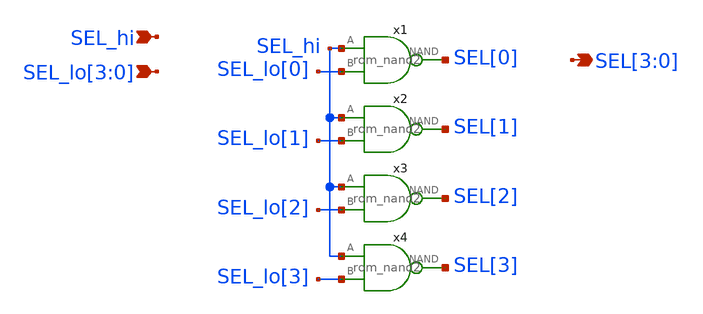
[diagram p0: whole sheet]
** sch_path: blocks/rom/rom_dec_nand.sch
**.subckt rom_dec_nand SEL[3],SEL[2],SEL[1],SEL[0] SEL_hi SEL_lo[3],SEL_lo[2],SEL_lo[1],SEL_lo[0]
*.opin SEL[3],SEL[2],SEL[1],SEL[0]
*.ipin SEL_hi
*.ipin SEL_lo[3],SEL_lo[2],SEL_lo[1],SEL_lo[0]
x2 SEL[1] SEL_hi SEL_lo[1] rom_nand2
x1 SEL[0] SEL_hi SEL_lo[0] rom_nand2
x4 SEL[3] SEL_hi SEL_lo[3] rom_nand2
x3 SEL[2] SEL_hi SEL_lo[2] rom_nand2
**.ends

* expanding   symbol:  rom_nand2.sym # of pins=3
** sym_path: blocks/rom/rom_nand2.sym
** sch_path: blocks/rom/rom_nand2.sch
.subckt rom_nand2 NAND A B
*.ipin A
*.opin NAND
*.ipin B
XM2 NAND B VCC VCC sky130_fd_pr__pfet_01v8 L=0.15 W=1 nf=1 ad='int((nf+1)/2) * W/nf * 0.29' as='int((nf+2)/2) * W/nf * 0.29'
+ pd='2*int((nf+1)/2) * (W/nf + 0.29)' ps='2*int((nf+2)/2) * (W/nf + 0.29)' nrd='0.29 / W' nrs='0.29 / W'
+ sa=0 sb=0 sd=0 mult=1 m=1
XM3 NAND A VCC VCC sky130_fd_pr__pfet_01v8 L=0.15 W=1 nf=1 ad='int((nf+1)/2) * W/nf * 0.29' as='int((nf+2)/2) * W/nf * 0.29'
+ pd='2*int((nf+1)/2) * (W/nf + 0.29)' ps='2*int((nf+2)/2) * (W/nf + 0.29)' nrd='0.29 / W' nrs='0.29 / W'
+ sa=0 sb=0 sd=0 mult=1 m=1
XM6 NAND A p0 VSS sky130_fd_pr__nfet_01v8 L=0.15 W=0.65 nf=1 ad='int((1 + 1)/2) * 0.65 / 1 * 0.29' as='int((1 + 2)/2) * 0.65 / 1 * 0.29'
+ pd='2*int((1 + 1)/2) * (0.65 / 1 + 0.29)' ps='2*int((1 + 2)/2) * (0.65 / 1 + 0.29)' nrd='0.29 / 0.65 '
+ nrs='0.29 / 0.65 ' sa=0 sb=0 sd=0 mult=1 m=1
XM7 p0 B VSS VSS sky130_fd_pr__nfet_01v8 L=0.15 W=0.65 nf=1 ad='int((1 + 1)/2) * 0.65 / 1 * 0.29' as='int((1 + 2)/2) * 0.65 / 1 * 0.29'
+ pd='2*int((1 + 1)/2) * (0.65 / 1 + 0.29)' ps='2*int((1 + 2)/2) * (0.65 / 1 + 0.29)' nrd='0.29 / 0.65 '
+ nrs='0.29 / 0.65 ' sa=0 sb=0 sd=0 mult=1 m=1
.ends

.GLOBAL VCC
.GLOBAL VSS
.end
